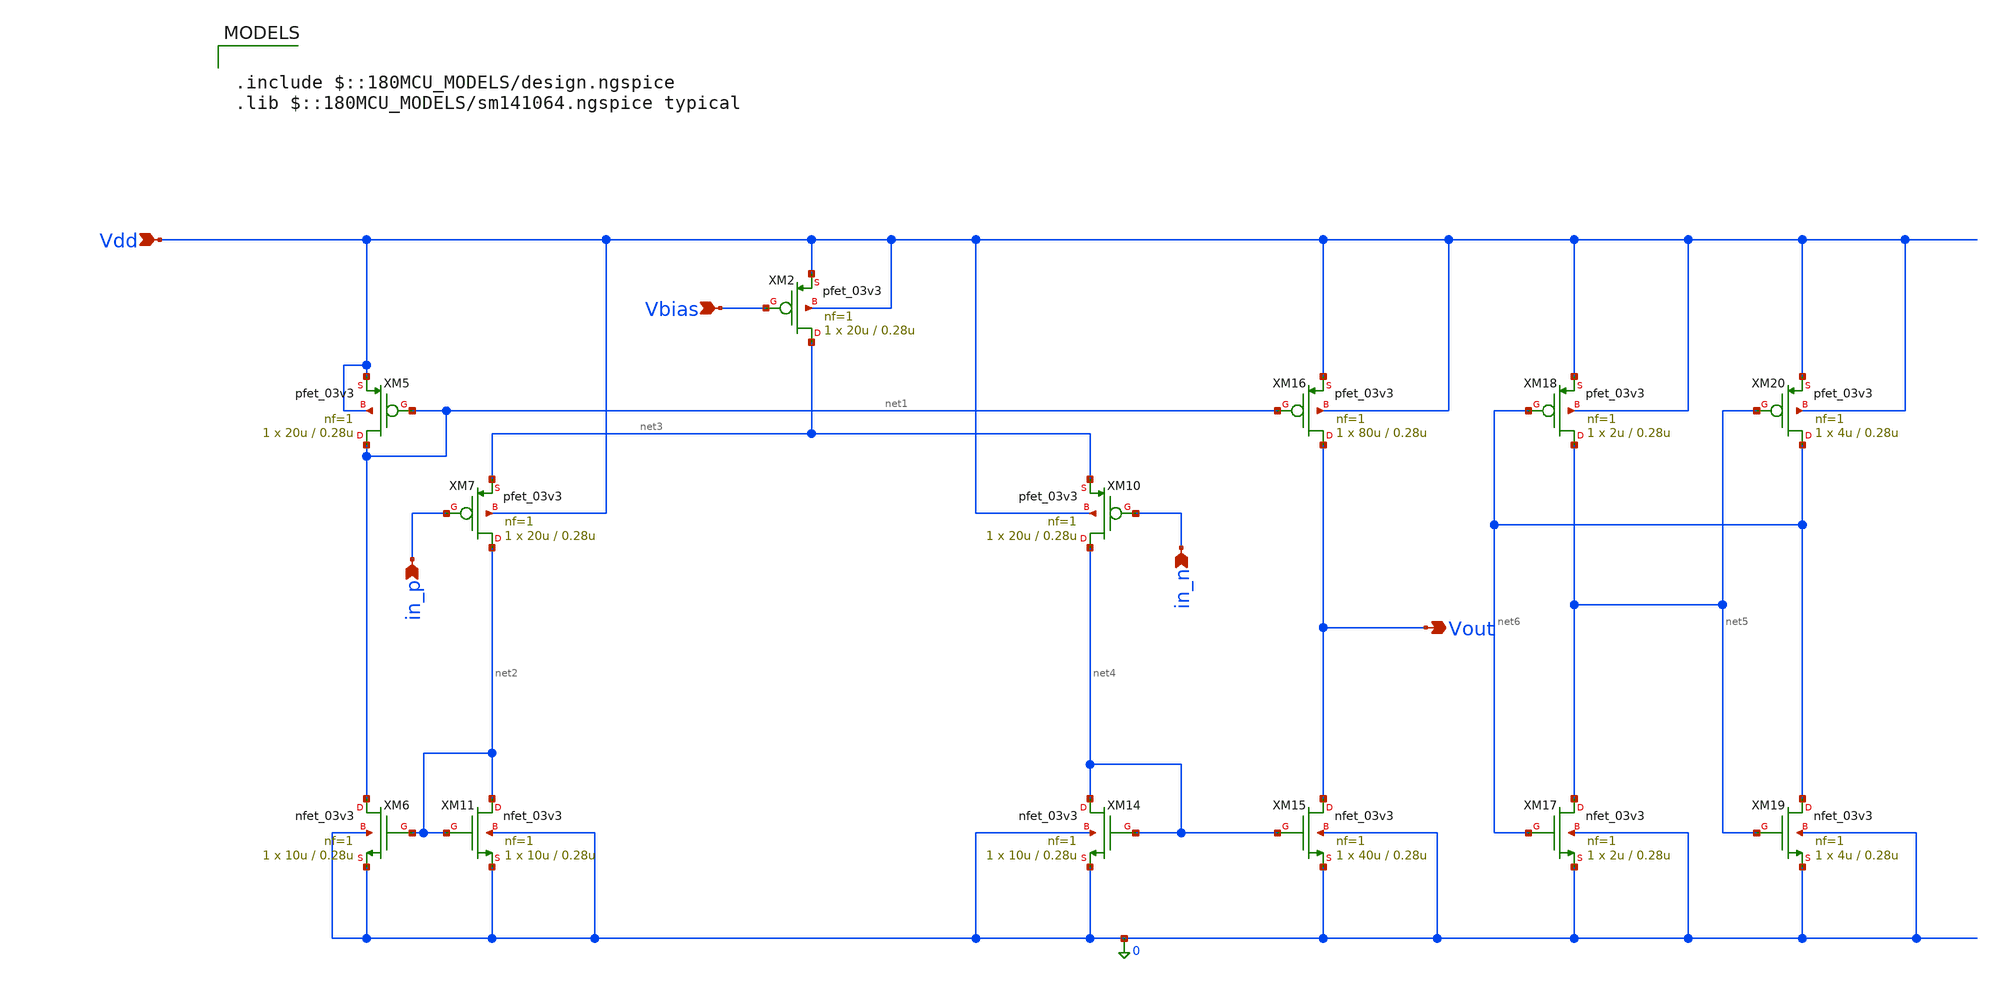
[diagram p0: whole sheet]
** sch_path: blocks/adc/lvds/lvds_rec_v2.sch
**.subckt lvds_rec_v2 Vdd in_n in_p Vout Vbias
*.ipin Vdd
*.ipin in_n
*.ipin in_p
*.opin Vout
*.ipin Vbias
XM2 net3 Vbias Vdd Vdd pfet_03v3 L=0.28u W=20u nf=1 ad='int((nf+1)/2) * W/nf * 0.18u' as='int((nf+2)/2) * W/nf * 0.18u'
+ pd='2*int((nf+1)/2) * (W/nf + 0.18u)' ps='2*int((nf+2)/2) * (W/nf + 0.18u)' nrd='0.18u / W' nrs='0.18u / W'
+ sa=0 sb=0 sd=0 m=1
XM5 net1 net1 Vdd Vdd pfet_03v3 L=0.28u W=20u nf=1 ad='int((nf+1)/2) * W/nf * 0.18u' as='int((nf+2)/2) * W/nf * 0.18u'
+ pd='2*int((nf+1)/2) * (W/nf + 0.18u)' ps='2*int((nf+2)/2) * (W/nf + 0.18u)' nrd='0.18u / W' nrs='0.18u / W'
+ sa=0 sb=0 sd=0 m=1
XM6 net1 net2 0 0 nfet_03v3 L=0.28u W=10u nf=1 ad='int((nf+1)/2) * W/nf * 0.18u' as='int((nf+2)/2) * W/nf * 0.18u'
+ pd='2*int((nf+1)/2) * (W/nf + 0.18u)' ps='2*int((nf+2)/2) * (W/nf + 0.18u)' nrd='0.18u / W' nrs='0.18u / W'
+ sa=0 sb=0 sd=0 m=1
XM7 net2 in_p net3 Vdd pfet_03v3 L=0.28u W=20u nf=1 ad='int((nf+1)/2) * W/nf * 0.18u' as='int((nf+2)/2) * W/nf * 0.18u'
+ pd='2*int((nf+1)/2) * (W/nf + 0.18u)' ps='2*int((nf+2)/2) * (W/nf + 0.18u)' nrd='0.18u / W' nrs='0.18u / W'
+ sa=0 sb=0 sd=0 m=1
XM10 net4 in_n net3 Vdd pfet_03v3 L=0.28u W=20u nf=1 ad='int((nf+1)/2) * W/nf * 0.18u' as='int((nf+2)/2) * W/nf * 0.18u'
+ pd='2*int((nf+1)/2) * (W/nf + 0.18u)' ps='2*int((nf+2)/2) * (W/nf + 0.18u)' nrd='0.18u / W' nrs='0.18u / W'
+ sa=0 sb=0 sd=0 m=1
XM11 net2 net2 0 0 nfet_03v3 L=0.28u W=10u nf=1 ad='int((nf+1)/2) * W/nf * 0.18u' as='int((nf+2)/2) * W/nf * 0.18u'
+ pd='2*int((nf+1)/2) * (W/nf + 0.18u)' ps='2*int((nf+2)/2) * (W/nf + 0.18u)' nrd='0.18u / W' nrs='0.18u / W'
+ sa=0 sb=0 sd=0 m=1
XM14 net4 net4 0 0 nfet_03v3 L=0.28u W=10u nf=1 ad='int((nf+1)/2) * W/nf * 0.18u' as='int((nf+2)/2) * W/nf * 0.18u'
+ pd='2*int((nf+1)/2) * (W/nf + 0.18u)' ps='2*int((nf+2)/2) * (W/nf + 0.18u)' nrd='0.18u / W' nrs='0.18u / W'
+ sa=0 sb=0 sd=0 m=1
XM15 Vout net4 0 0 nfet_03v3 L=0.28u W=40u nf=1 ad='int((nf+1)/2) * W/nf * 0.18u' as='int((nf+2)/2) * W/nf * 0.18u'
+ pd='2*int((nf+1)/2) * (W/nf + 0.18u)' ps='2*int((nf+2)/2) * (W/nf + 0.18u)' nrd='0.18u / W' nrs='0.18u / W'
+ sa=0 sb=0 sd=0 m=1
XM16 Vout net1 Vdd Vdd pfet_03v3 L=0.28u W=80u nf=1 ad='int((nf+1)/2) * W/nf * 0.18u' as='int((nf+2)/2) * W/nf * 0.18u'
+ pd='2*int((nf+1)/2) * (W/nf + 0.18u)' ps='2*int((nf+2)/2) * (W/nf + 0.18u)' nrd='0.18u / W' nrs='0.18u / W'
+ sa=0 sb=0 sd=0 m=1
XM17 net5 net6 0 0 nfet_03v3 L=0.28u W=2u nf=1 ad='int((nf+1)/2) * W/nf * 0.18u' as='int((nf+2)/2) * W/nf * 0.18u'
+ pd='2*int((nf+1)/2) * (W/nf + 0.18u)' ps='2*int((nf+2)/2) * (W/nf + 0.18u)' nrd='0.18u / W' nrs='0.18u / W'
+ sa=0 sb=0 sd=0 m=1
XM18 net5 net6 Vdd Vdd pfet_03v3 L=0.28u W=2u nf=1 ad='int((nf+1)/2) * W/nf * 0.18u' as='int((nf+2)/2) * W/nf * 0.18u'
+ pd='2*int((nf+1)/2) * (W/nf + 0.18u)' ps='2*int((nf+2)/2) * (W/nf + 0.18u)' nrd='0.18u / W' nrs='0.18u / W'
+ sa=0 sb=0 sd=0 m=1
XM19 net6 net5 0 0 nfet_03v3 L=0.28u W=4u nf=1 ad='int((nf+1)/2) * W/nf * 0.18u' as='int((nf+2)/2) * W/nf * 0.18u'
+ pd='2*int((nf+1)/2) * (W/nf + 0.18u)' ps='2*int((nf+2)/2) * (W/nf + 0.18u)' nrd='0.18u / W' nrs='0.18u / W'
+ sa=0 sb=0 sd=0 m=1
XM20 net6 net5 Vdd Vdd pfet_03v3 L=0.28u W=4u nf=1 ad='int((nf+1)/2) * W/nf * 0.18u' as='int((nf+2)/2) * W/nf * 0.18u'
+ pd='2*int((nf+1)/2) * (W/nf + 0.18u)' ps='2*int((nf+2)/2) * (W/nf + 0.18u)' nrd='0.18u / W' nrs='0.18u / W'
+ sa=0 sb=0 sd=0 m=1
**** begin user architecture code

.include $::180MCU_MODELS/design.ngspice
.lib $::180MCU_MODELS/sm141064.ngspice typical

**** end user architecture code
**.ends
.end
